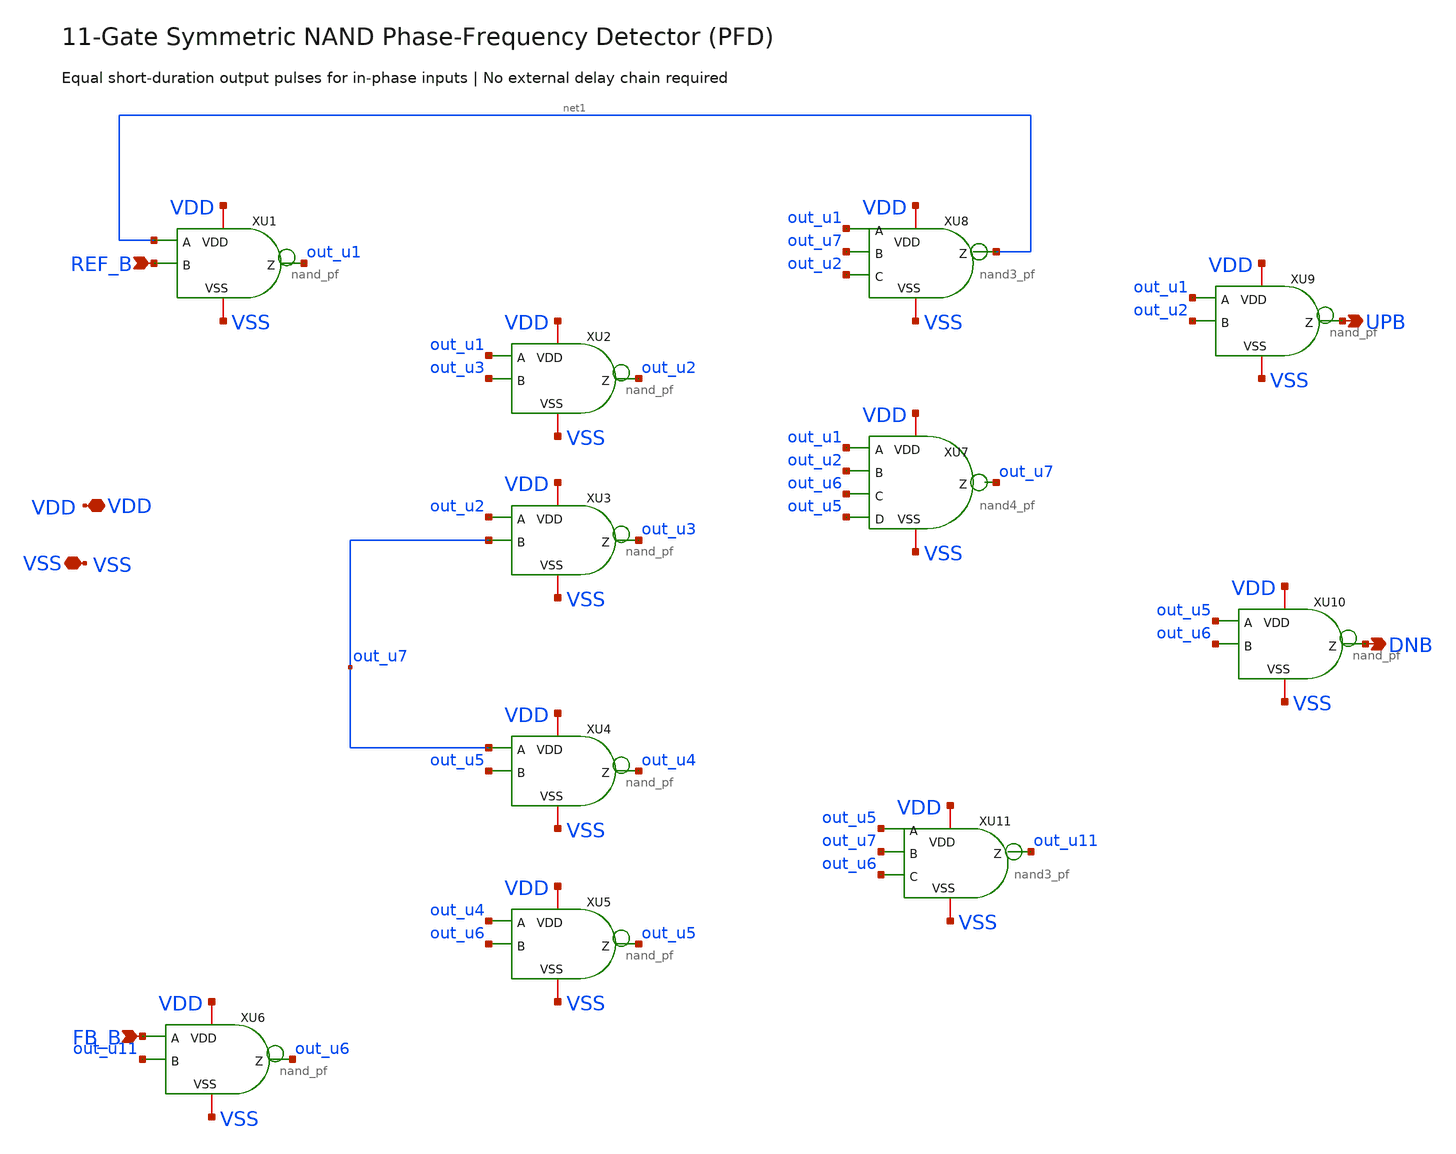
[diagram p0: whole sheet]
** sch_path: designs/libs/core_analog/pfd/pfd_11gate.sch
**.subckt pfd_11gate REF_B FB_B UPB DNB VDD VSS
*.ipin REF_B
*.ipin FB_B
*.opin UPB
*.opin DNB
*.iopin VDD
*.iopin VSS
XU1 VDD out_u1 net1 REF_B VSS nand_pf
XU2 VDD out_u2 out_u1 out_u3 VSS nand_pf
XU3 VDD out_u3 out_u2 out_u7 VSS nand_pf
XU4 VDD out_u4 out_u7 out_u5 VSS nand_pf
XU5 VDD out_u5 out_u4 out_u6 VSS nand_pf
XU6 VDD out_u6 FB_B out_u11 VSS nand_pf
XU7 VDD out_u7 out_u1 out_u2 out_u6 out_u5 VSS nand4_pf
XU8 VDD net1 out_u1 out_u7 out_u2 VSS nand3_pf
XU9 VDD UPB out_u1 out_u2 VSS nand_pf
XU10 VDD DNB out_u5 out_u6 VSS nand_pf
XU11 VDD out_u11 out_u5 out_u7 out_u6 VSS nand3_pf
**.ends
.end
